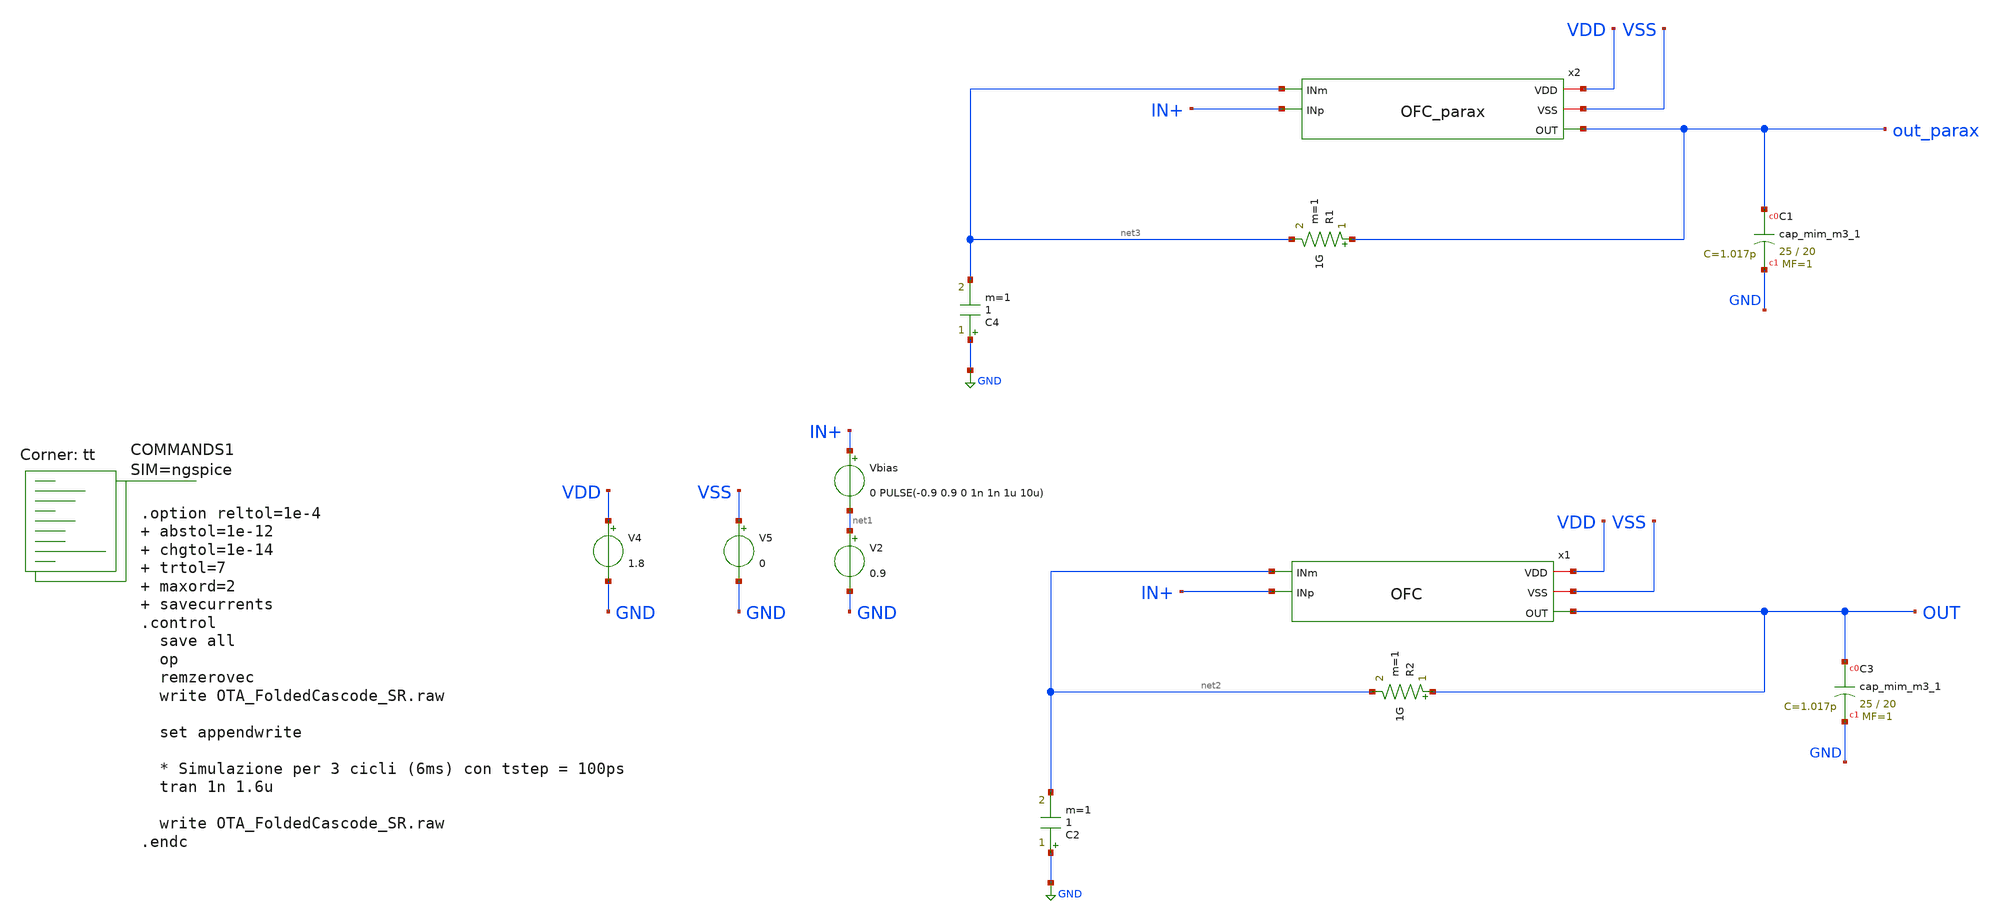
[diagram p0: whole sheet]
** sch_path: tt_um_NE567Mixer28/xschem/OTA_FoldedCascode_SR.sch
**.subckt OTA_FoldedCascode_SR
Vbias IN+ net1 0 PULSE(-0.9 0.9 0 1n 1n 1u 10u)
V2 net1 GND 0.9
x1 VDD VSS OUT net2 IN+ OFC
XC3 OUT GND sky130_fd_pr__cap_mim_m3_1 W=25 L=20 MF=1 m=1
C2 GND net2 1 m=1
R2 OUT net2 1G m=1
V4 VDD GND 1.8
V5 VSS GND 0
x2 VDD VSS out_parax net3 IN+ OFC_parax
XC1 out_parax GND sky130_fd_pr__cap_mim_m3_1 W=25 L=20 MF=1 m=1
C4 GND net3 1 m=1
R1 out_parax net3 1G m=1
**** begin user architecture code



.option reltol=1e-4  abstol=1e-12  chgtol=1e-14  trtol=7  maxord=2  savecurrents
.control
  save all
  op
  remzerovec
  write OTA_FoldedCascode_SR.raw

  set appendwrite

  * Simulazione per 3 cicli (6ms) con tstep = 100ps
  tran 1n 1.6u

  write OTA_FoldedCascode_SR.raw
.endc



.lib $::SKYWATER_MODELS/sky130.lib.spice tt
**** end user architecture code
**.ends

* expanding   symbol:  OFC.sym # of pins=5
** sym_path: tt_um_NE567Mixer28/xschem/OFC.sym
** sch_path: tt_um_NE567Mixer28/xschem/OFC.sch
.subckt OFC VDD VSS OUT INm INp
*.iopin VDD
*.iopin VSS
*.ipin INp
*.ipin INm
*.opin OUT
XM11 S Vb VDD VDD sky130_fd_pr__pfet_01v8_lvt L=1 W=60 nf=6 ad='int((nf+1)/2) * W/nf * 0.29' as='int((nf+2)/2) * W/nf * 0.29'
+ pd='2*int((nf+1)/2) * (W/nf + 0.29)' ps='2*int((nf+2)/2) * (W/nf + 0.29)' nrd='0.29 / W' nrs='0.29 / W'
+ sa=0 sb=0 sd=0 mult=2 m=2
XM1 D1 INp S S sky130_fd_pr__pfet_01v8_lvt L=10 W=25 nf=2 ad='int((nf+1)/2) * W/nf * 0.29' as='int((nf+2)/2) * W/nf * 0.29'
+ pd='2*int((nf+1)/2) * (W/nf + 0.29)' ps='2*int((nf+2)/2) * (W/nf + 0.29)' nrd='0.29 / W' nrs='0.29 / W'
+ sa=0 sb=0 sd=0 mult=2 m=2
XM2 D2 INm S S sky130_fd_pr__pfet_01v8_lvt L=10 W=25 nf=2 ad='int((nf+1)/2) * W/nf * 0.29' as='int((nf+2)/2) * W/nf * 0.29'
+ pd='2*int((nf+1)/2) * (W/nf + 0.29)' ps='2*int((nf+2)/2) * (W/nf + 0.29)' nrd='0.29 / W' nrs='0.29 / W'
+ sa=0 sb=0 sd=0 mult=2 m=2
XM3 OUT Vc1 D2 VSS sky130_fd_pr__nfet_01v8_lvt L=1 W=4 nf=1 ad='int((nf+1)/2) * W/nf * 0.29' as='int((nf+2)/2) * W/nf * 0.29'
+ pd='2*int((nf+1)/2) * (W/nf + 0.29)' ps='2*int((nf+2)/2) * (W/nf + 0.29)' nrd='0.29 / W' nrs='0.29 / W'
+ sa=0 sb=0 sd=0 mult=1 m=1
XM4 D2 Vc VSS VSS sky130_fd_pr__nfet_01v8_lvt L=1 W=2.8 nf=1 ad='int((nf+1)/2) * W/nf * 0.29' as='int((nf+2)/2) * W/nf * 0.29'
+ pd='2*int((nf+1)/2) * (W/nf + 0.29)' ps='2*int((nf+2)/2) * (W/nf + 0.29)' nrd='0.29 / W' nrs='0.29 / W'
+ sa=0 sb=0 sd=0 mult=1 m=1
XM5 D1 Vc VSS VSS sky130_fd_pr__nfet_01v8_lvt L=1 W=2.8 nf=1 ad='int((nf+1)/2) * W/nf * 0.29' as='int((nf+2)/2) * W/nf * 0.29'
+ pd='2*int((nf+1)/2) * (W/nf + 0.29)' ps='2*int((nf+2)/2) * (W/nf + 0.29)' nrd='0.29 / W' nrs='0.29 / W'
+ sa=0 sb=0 sd=0 mult=1 m=1
XM6 G Vc1 D1 VSS sky130_fd_pr__nfet_01v8_lvt L=1 W=4 nf=1 ad='int((nf+1)/2) * W/nf * 0.29' as='int((nf+2)/2) * W/nf * 0.29'
+ pd='2*int((nf+1)/2) * (W/nf + 0.29)' ps='2*int((nf+2)/2) * (W/nf + 0.29)' nrd='0.29 / W' nrs='0.29 / W'
+ sa=0 sb=0 sd=0 mult=1 m=1
XM7 G Vc2 D9 D9 sky130_fd_pr__pfet_01v8_lvt L=2.23 W=3 nf=1 ad='int((nf+1)/2) * W/nf * 0.29' as='int((nf+2)/2) * W/nf * 0.29'
+ pd='2*int((nf+1)/2) * (W/nf + 0.29)' ps='2*int((nf+2)/2) * (W/nf + 0.29)' nrd='0.29 / W' nrs='0.29 / W'
+ sa=0 sb=0 sd=0 mult=1 m=1
XM9 D9 G VDD VDD sky130_fd_pr__pfet_01v8_lvt L=2.23 W=4 nf=1 ad='int((nf+1)/2) * W/nf * 0.29' as='int((nf+2)/2) * W/nf * 0.29'
+ pd='2*int((nf+1)/2) * (W/nf + 0.29)' ps='2*int((nf+2)/2) * (W/nf + 0.29)' nrd='0.29 / W' nrs='0.29 / W'
+ sa=0 sb=0 sd=0 mult=1 m=1
XM8 D10 G VDD VDD sky130_fd_pr__pfet_01v8_lvt L=2.23 W=4 nf=1 ad='int((nf+1)/2) * W/nf * 0.29' as='int((nf+2)/2) * W/nf * 0.29'
+ pd='2*int((nf+1)/2) * (W/nf + 0.29)' ps='2*int((nf+2)/2) * (W/nf + 0.29)' nrd='0.29 / W' nrs='0.29 / W'
+ sa=0 sb=0 sd=0 mult=1 m=1
XM10 OUT Vc2 D10 D10 sky130_fd_pr__pfet_01v8_lvt L=2.23 W=3 nf=1 ad='int((nf+1)/2) * W/nf * 0.29' as='int((nf+2)/2) * W/nf * 0.29'
+ pd='2*int((nf+1)/2) * (W/nf + 0.29)' ps='2*int((nf+2)/2) * (W/nf + 0.29)' nrd='0.29 / W' nrs='0.29 / W'
+ sa=0 sb=0 sd=0 mult=1 m=1
XR2 Vb VDD VSS sky130_fd_pr__res_xhigh_po_0p35 L=5 mult=1 m=1
XR3 VSS Vb VSS sky130_fd_pr__res_xhigh_po_0p35 L=13.2 mult=1 m=1
XR1 Vc VDD VSS sky130_fd_pr__res_xhigh_po_0p35 L=5 mult=1 m=1
XR4 VSS Vc VSS sky130_fd_pr__res_xhigh_po_0p35 L=3.07 mult=1 m=1
XR5 Vc1 VDD VSS sky130_fd_pr__res_xhigh_po_0p35 L=5 mult=1 m=1
XR6 VSS Vc1 VSS sky130_fd_pr__res_xhigh_po_0p35 L=13.2 mult=1 m=1
XR7 Vc2 VDD VSS sky130_fd_pr__res_xhigh_po_0p35 L=5 mult=1 m=1
XR8 VSS Vc2 VSS sky130_fd_pr__res_xhigh_po_0p35 L=1.6 mult=1 m=1
.ends


* expanding   symbol:  OFC_parax.sym # of pins=5
** sym_path: tt_um_NE567Mixer28/xschem/OFC.sym
.include [file normalize ../mag/OFC.sim.spice]
.GLOBAL GND
.end
